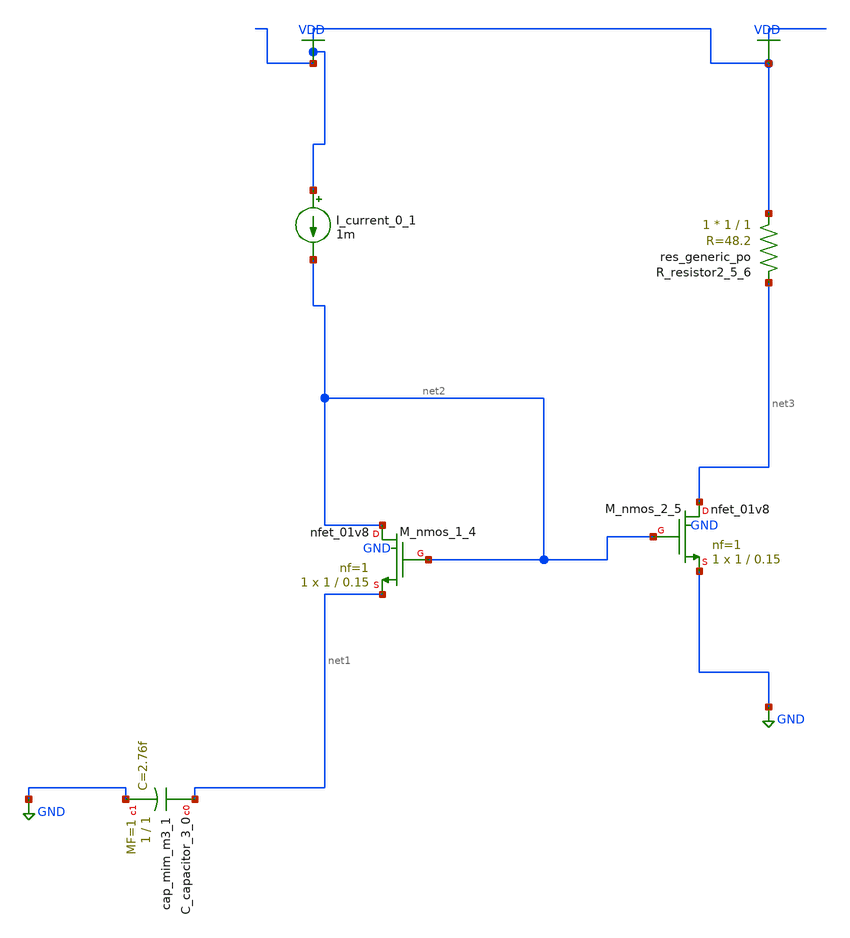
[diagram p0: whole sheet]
** sch_path: schematics/AMSNet/337.sch
**.subckt 337
XC_capacitor_3_0 net1 GND sky130_fd_pr__cap_mim_m3_1 W=1 L=1 MF=1 m=1
I_current_0_1 VDD net2 1m
XM_nmos_1_4 net2 net2 net1 GND sky130_fd_pr__nfet_01v8 L=0.15 W=1 nf=1 ad='int((1 + 1)/2) * 1 / 1 * 0.29'
+ as='int((1 + 2)/2) * 1 / 1 * 0.29' pd='2*int((1 + 1)/2) * (1 / 1 + 0.29)' ps='2*int((1 + 2)/2) * (1 / 1 + 0.29)'
+ nrd='0.29 / 1 ' nrs='0.29 / 1 ' sa=0 sb=0 sd=0 mult=1 m=1
XM_nmos_2_5 net3 net2 GND GND sky130_fd_pr__nfet_01v8 L=0.15 W=1 nf=1 ad='int((1 + 1)/2) * 1 / 1 * 0.29'
+ as='int((1 + 2)/2) * 1 / 1 * 0.29' pd='2*int((1 + 1)/2) * (1 / 1 + 0.29)' ps='2*int((1 + 2)/2) * (1 / 1 + 0.29)'
+ nrd='0.29 / 1 ' nrs='0.29 / 1 ' sa=0 sb=0 sd=0 mult=1 m=1
XR_resistor2_5_6 VDD net3 sky130_fd_pr__res_generic_po W=1 L=1 m=1
**.ends
.GLOBAL GND
.GLOBAL VDD
.end
